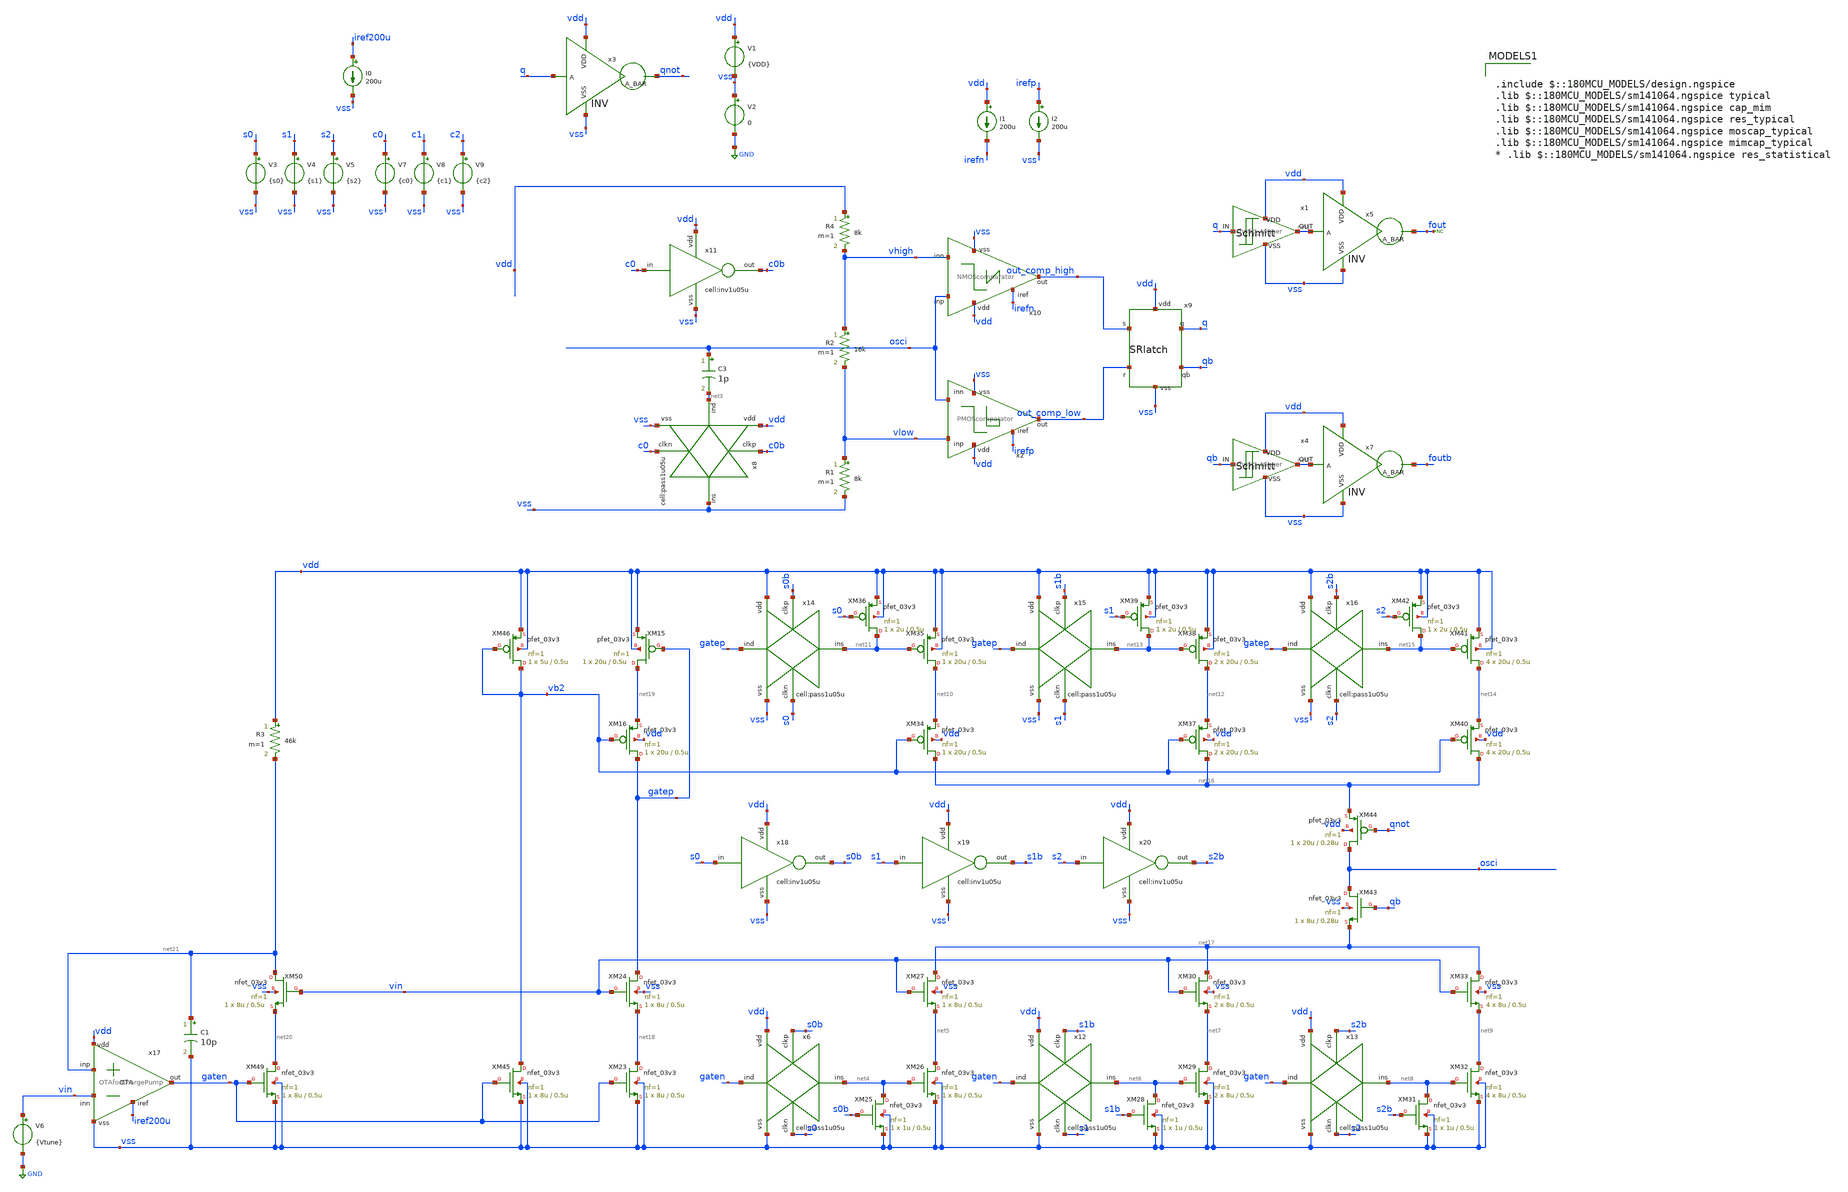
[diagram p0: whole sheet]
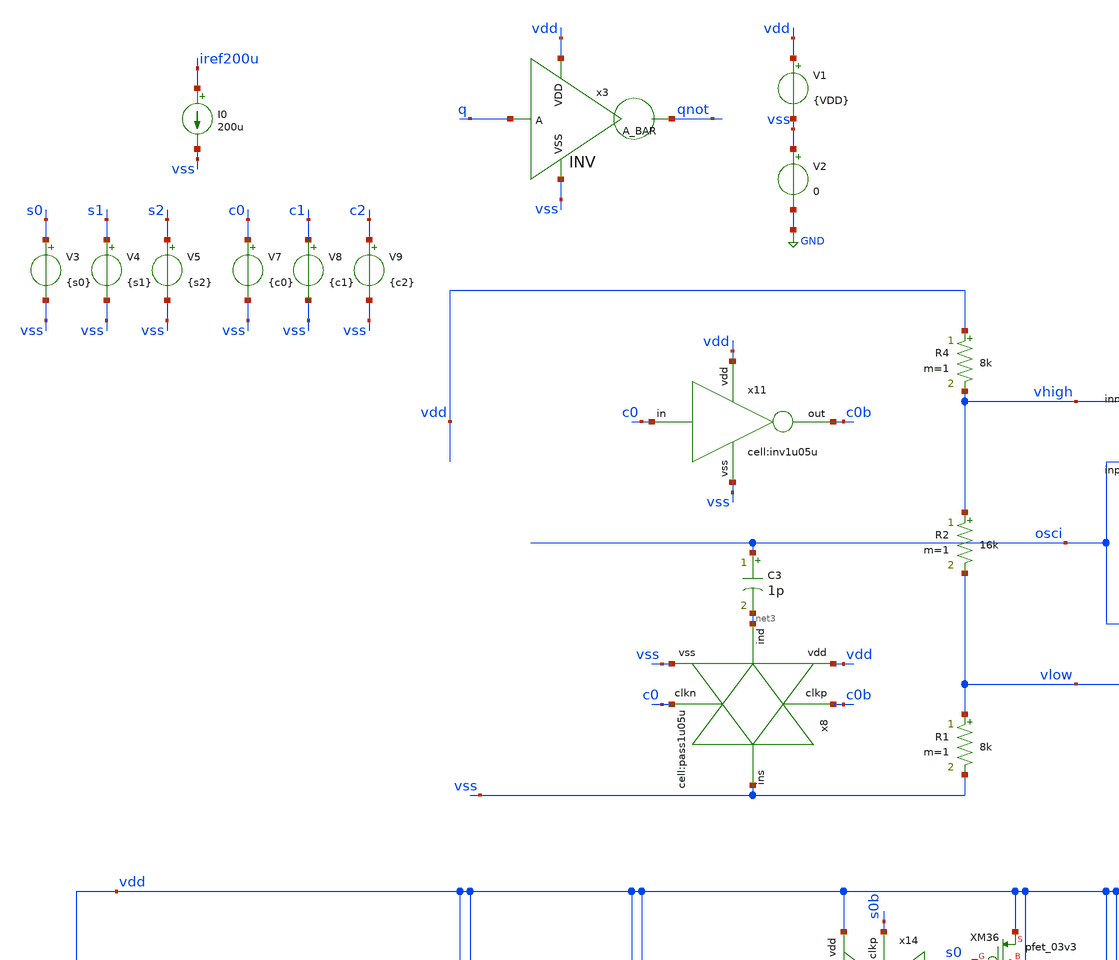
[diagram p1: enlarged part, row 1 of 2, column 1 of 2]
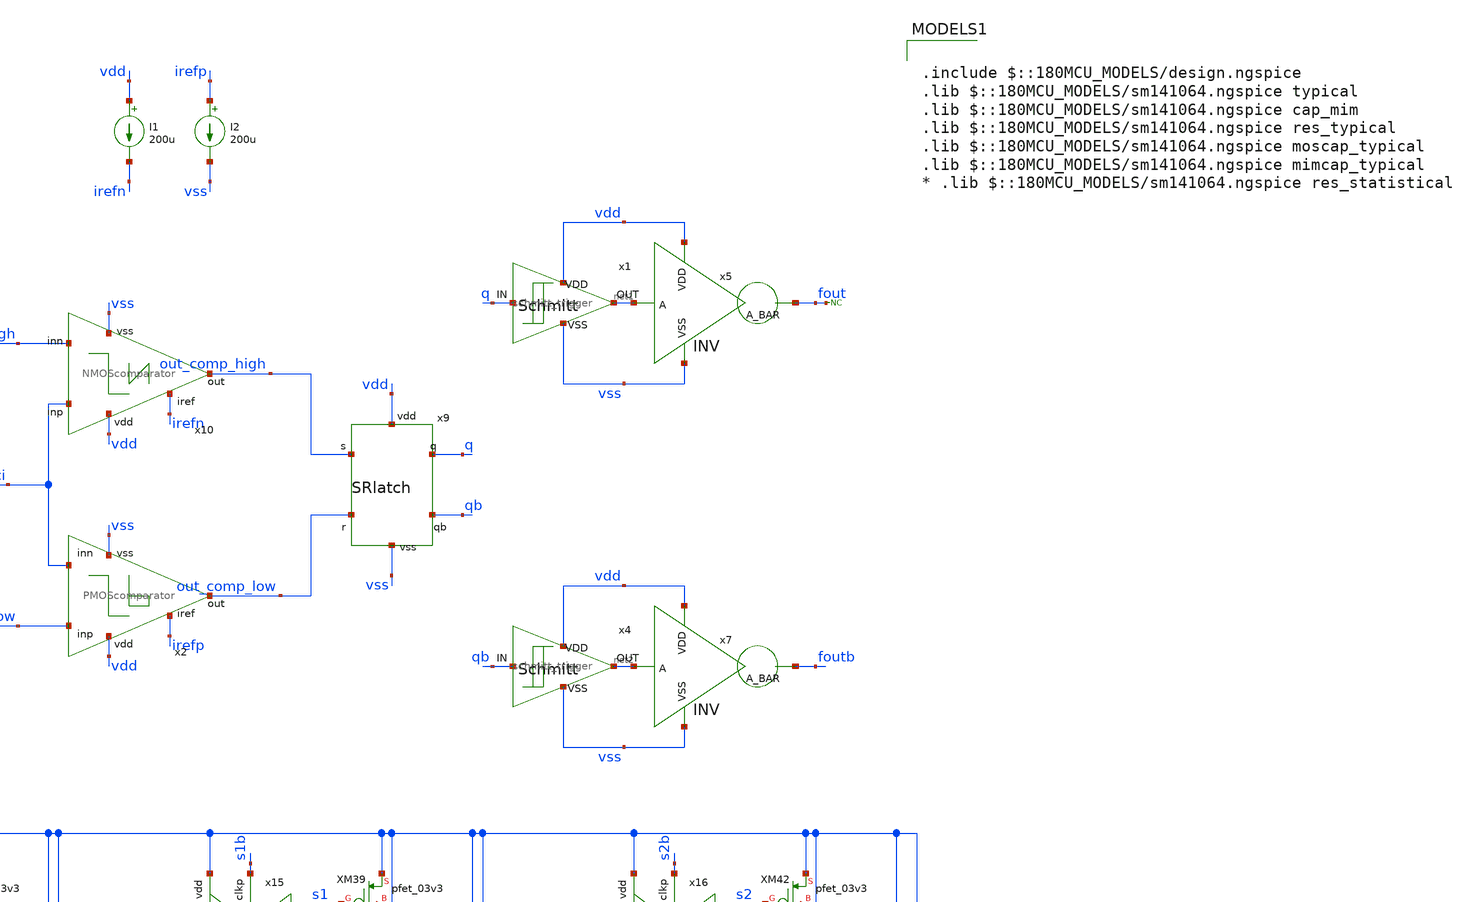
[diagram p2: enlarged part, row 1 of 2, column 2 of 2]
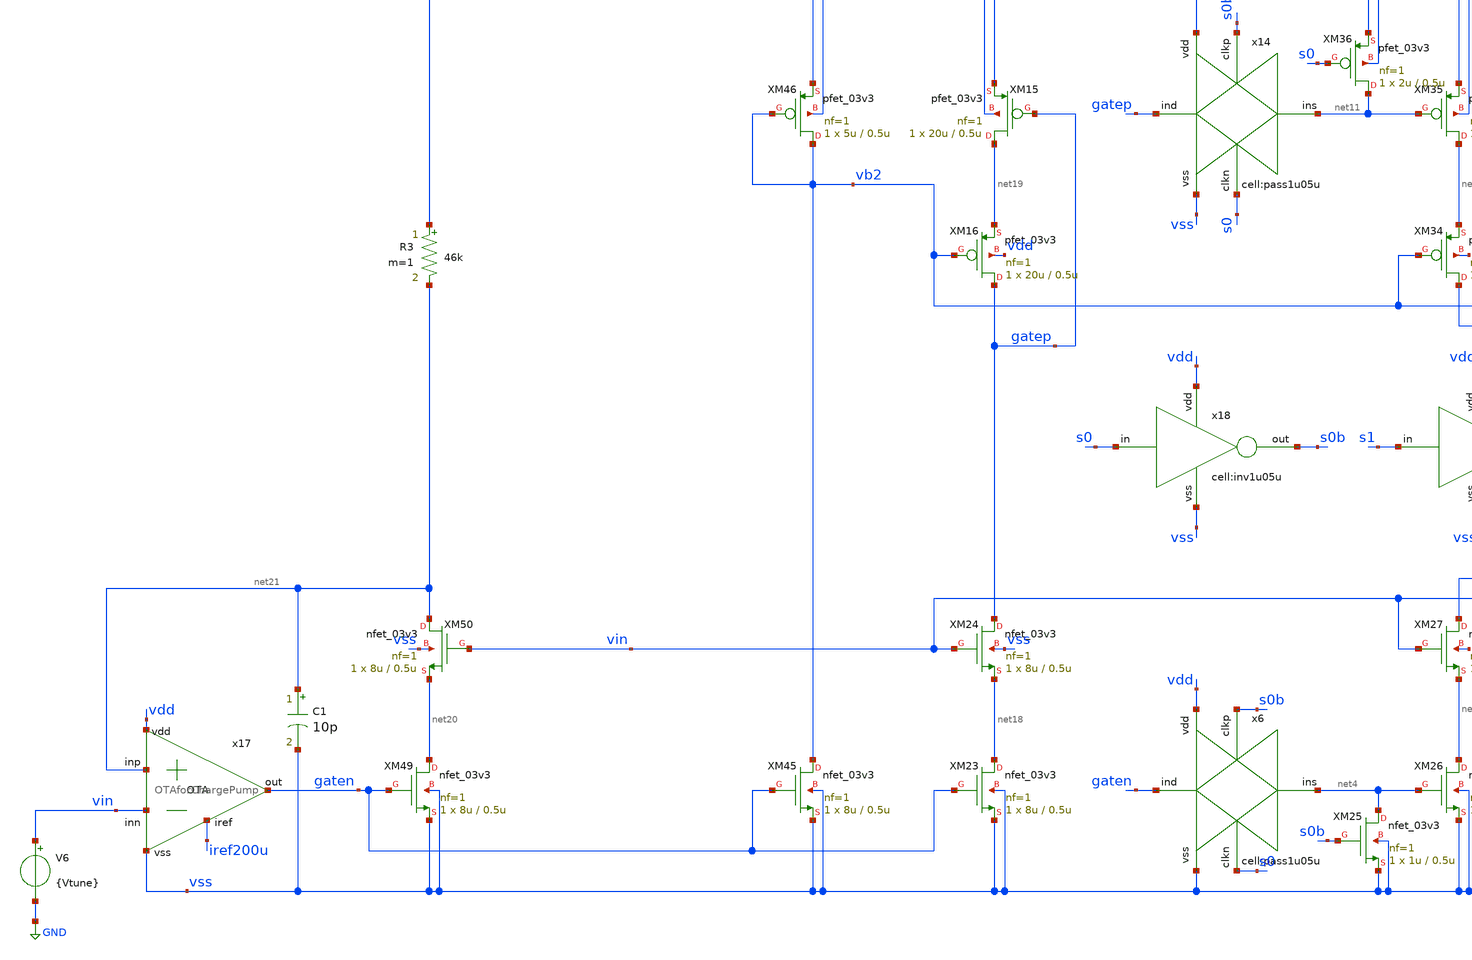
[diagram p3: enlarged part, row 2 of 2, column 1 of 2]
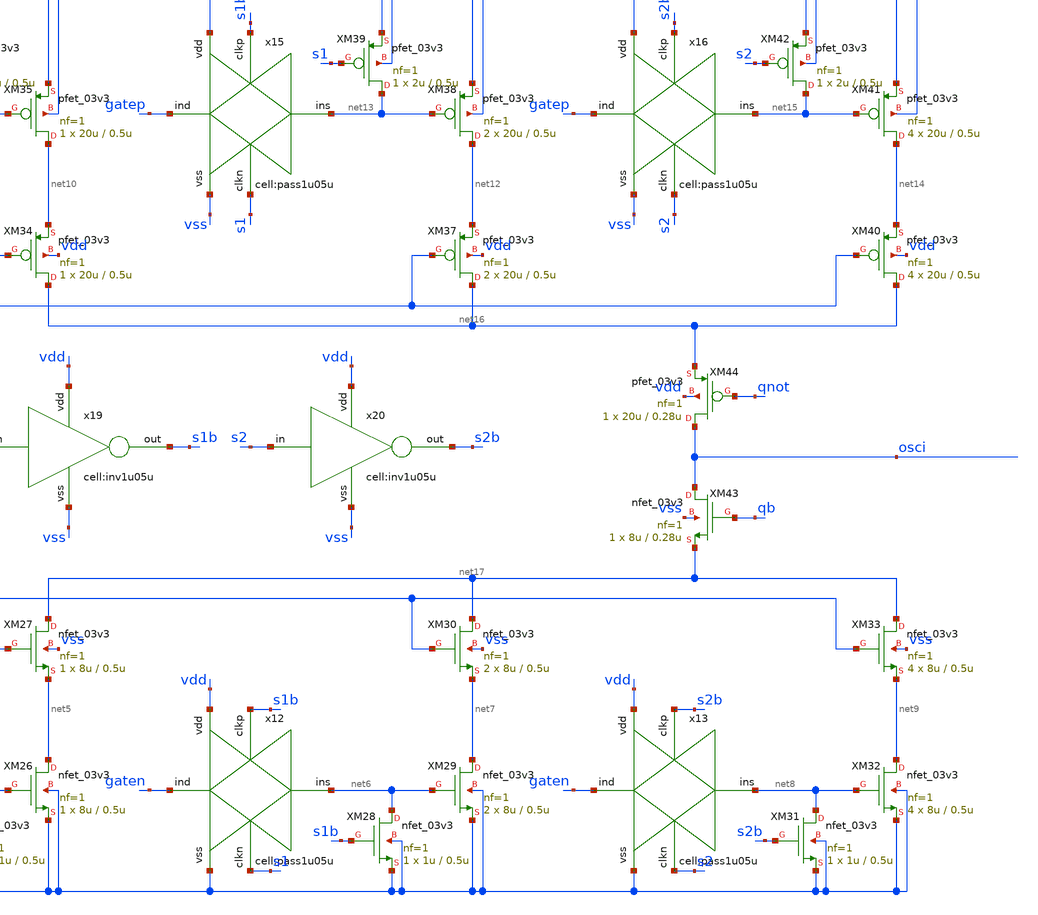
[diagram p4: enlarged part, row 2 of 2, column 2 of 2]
** sch_path: designs/libs/qw_core_analog/VCO0826/VCO0826.sch
**.subckt VCO0826
V1 vdd vss {VDD}
V2 vss GND 0
I1 vdd irefn 200u
I2 irefp vss 200u
R1 vlow vss 8k m=1
R2 vhigh vlow 16k m=1
R4 vdd vhigh 8k m=1
x9 vdd out_comp_high q qb out_comp_low vss SRlatch
x2 vdd irefp vlow out_comp_low osci vss PMOScomparator
x10 vdd osci out_comp_high vhigh irefn vss NMOScomparator
x3 vdd q qnot vss INV
x1 q net1 vdd vss schmitt_trigger
x4 qb net2 vdd vss schmitt_trigger
x5 vdd net1 fout vss INV
x7 vdd net2 foutb vss INV
V6 vin GND {Vtune}
I0 iref200u vss 200u
* noconn fout
V3 s0 vss {s0}
V4 s1 vss {s1}
V5 s2 vss {s2}
V7 c0 vss {c0}
V8 c1 vss {c1}
V9 c2 vss {c2}
C3 osci net3 1p m=1
x8 net3 vss c0 vss c0b vdd pass1u05u
x11 c0 vdd c0b vss inv1u05u
x6 gaten vss s0 net4 s0b vdd pass1u05u
XM25 net4 s0b vss vss nfet_03v3 L=0.5u W=1u nf=1 ad='int((nf+1)/2) * W/nf * 0.18u' as='int((nf+2)/2) * W/nf * 0.18u'
+ pd='2*int((nf+1)/2) * (W/nf + 0.18u)' ps='2*int((nf+2)/2) * (W/nf + 0.18u)' nrd='0.18u / W' nrs='0.18u / W'
+ sa=0 sb=0 sd=0 m=1
XM26 net5 net4 vss vss nfet_03v3 L=0.5u W=8u nf=1 ad='int((nf+1)/2) * W/nf * 0.18u' as='int((nf+2)/2) * W/nf * 0.18u'
+ pd='2*int((nf+1)/2) * (W/nf + 0.18u)' ps='2*int((nf+2)/2) * (W/nf + 0.18u)' nrd='0.18u / W' nrs='0.18u / W'
+ sa=0 sb=0 sd=0 m=1
XM27 net17 vin net5 vss nfet_03v3 L=0.5u W=8u nf=1 ad='int((nf+1)/2) * W/nf * 0.18u' as='int((nf+2)/2) * W/nf * 0.18u'
+ pd='2*int((nf+1)/2) * (W/nf + 0.18u)' ps='2*int((nf+2)/2) * (W/nf + 0.18u)' nrd='0.18u / W' nrs='0.18u / W'
+ sa=0 sb=0 sd=0 m=1
x12 gaten vss s1 net6 s1b vdd pass1u05u
XM28 net6 s1b vss vss nfet_03v3 L=0.5u W=1u nf=1 ad='int((nf+1)/2) * W/nf * 0.18u' as='int((nf+2)/2) * W/nf * 0.18u'
+ pd='2*int((nf+1)/2) * (W/nf + 0.18u)' ps='2*int((nf+2)/2) * (W/nf + 0.18u)' nrd='0.18u / W' nrs='0.18u / W'
+ sa=0 sb=0 sd=0 m=1
XM29 net7 net6 vss vss nfet_03v3 L=0.5u W=8u nf=1 ad='int((nf+1)/2) * W/nf * 0.18u' as='int((nf+2)/2) * W/nf * 0.18u'
+ pd='2*int((nf+1)/2) * (W/nf + 0.18u)' ps='2*int((nf+2)/2) * (W/nf + 0.18u)' nrd='0.18u / W' nrs='0.18u / W'
+ sa=0 sb=0 sd=0 m=2
XM30 net17 vin net7 vss nfet_03v3 L=0.5u W=8u nf=1 ad='int((nf+1)/2) * W/nf * 0.18u' as='int((nf+2)/2) * W/nf * 0.18u'
+ pd='2*int((nf+1)/2) * (W/nf + 0.18u)' ps='2*int((nf+2)/2) * (W/nf + 0.18u)' nrd='0.18u / W' nrs='0.18u / W'
+ sa=0 sb=0 sd=0 m=2
x13 gaten vss s2 net8 s2b vdd pass1u05u
XM31 net8 s2b vss vss nfet_03v3 L=0.5u W=1u nf=1 ad='int((nf+1)/2) * W/nf * 0.18u' as='int((nf+2)/2) * W/nf * 0.18u'
+ pd='2*int((nf+1)/2) * (W/nf + 0.18u)' ps='2*int((nf+2)/2) * (W/nf + 0.18u)' nrd='0.18u / W' nrs='0.18u / W'
+ sa=0 sb=0 sd=0 m=1
XM32 net9 net8 vss vss nfet_03v3 L=0.5u W=8u nf=1 ad='int((nf+1)/2) * W/nf * 0.18u' as='int((nf+2)/2) * W/nf * 0.18u'
+ pd='2*int((nf+1)/2) * (W/nf + 0.18u)' ps='2*int((nf+2)/2) * (W/nf + 0.18u)' nrd='0.18u / W' nrs='0.18u / W'
+ sa=0 sb=0 sd=0 m=4
XM33 net17 vin net9 vss nfet_03v3 L=0.5u W=8u nf=1 ad='int((nf+1)/2) * W/nf * 0.18u' as='int((nf+2)/2) * W/nf * 0.18u'
+ pd='2*int((nf+1)/2) * (W/nf + 0.18u)' ps='2*int((nf+2)/2) * (W/nf + 0.18u)' nrd='0.18u / W' nrs='0.18u / W'
+ sa=0 sb=0 sd=0 m=4
XM34 net16 vb2 net10 vdd pfet_03v3 L=0.5u W=20u nf=1 ad='int((nf+1)/2) * W/nf * 0.18u' as='int((nf+2)/2) * W/nf * 0.18u'
+ pd='2*int((nf+1)/2) * (W/nf + 0.18u)' ps='2*int((nf+2)/2) * (W/nf + 0.18u)' nrd='0.18u / W' nrs='0.18u / W'
+ sa=0 sb=0 sd=0 m=1
XM35 net10 net11 vdd vdd pfet_03v3 L=0.5u W=20u nf=1 ad='int((nf+1)/2) * W/nf * 0.18u' as='int((nf+2)/2) * W/nf * 0.18u'
+ pd='2*int((nf+1)/2) * (W/nf + 0.18u)' ps='2*int((nf+2)/2) * (W/nf + 0.18u)' nrd='0.18u / W' nrs='0.18u / W'
+ sa=0 sb=0 sd=0 m=1
x14 gatep vss s0 net11 s0b vdd pass1u05u
XM36 net11 s0 vdd vdd pfet_03v3 L=0.5u W=2u nf=1 ad='int((nf+1)/2) * W/nf * 0.18u' as='int((nf+2)/2) * W/nf * 0.18u'
+ pd='2*int((nf+1)/2) * (W/nf + 0.18u)' ps='2*int((nf+2)/2) * (W/nf + 0.18u)' nrd='0.18u / W' nrs='0.18u / W'
+ sa=0 sb=0 sd=0 m=1
XM37 net16 vb2 net12 vdd pfet_03v3 L=0.5u W=20u nf=1 ad='int((nf+1)/2) * W/nf * 0.18u' as='int((nf+2)/2) * W/nf * 0.18u'
+ pd='2*int((nf+1)/2) * (W/nf + 0.18u)' ps='2*int((nf+2)/2) * (W/nf + 0.18u)' nrd='0.18u / W' nrs='0.18u / W'
+ sa=0 sb=0 sd=0 m=2
XM38 net12 net13 vdd vdd pfet_03v3 L=0.5u W=20u nf=1 ad='int((nf+1)/2) * W/nf * 0.18u' as='int((nf+2)/2) * W/nf * 0.18u'
+ pd='2*int((nf+1)/2) * (W/nf + 0.18u)' ps='2*int((nf+2)/2) * (W/nf + 0.18u)' nrd='0.18u / W' nrs='0.18u / W'
+ sa=0 sb=0 sd=0 m=2
x15 gatep vss s1 net13 s1b vdd pass1u05u
XM39 net13 s1 vdd vdd pfet_03v3 L=0.5u W=2u nf=1 ad='int((nf+1)/2) * W/nf * 0.18u' as='int((nf+2)/2) * W/nf * 0.18u'
+ pd='2*int((nf+1)/2) * (W/nf + 0.18u)' ps='2*int((nf+2)/2) * (W/nf + 0.18u)' nrd='0.18u / W' nrs='0.18u / W'
+ sa=0 sb=0 sd=0 m=1
XM40 net16 vb2 net14 vdd pfet_03v3 L=0.5u W=20u nf=1 ad='int((nf+1)/2) * W/nf * 0.18u' as='int((nf+2)/2) * W/nf * 0.18u'
+ pd='2*int((nf+1)/2) * (W/nf + 0.18u)' ps='2*int((nf+2)/2) * (W/nf + 0.18u)' nrd='0.18u / W' nrs='0.18u / W'
+ sa=0 sb=0 sd=0 m=4
XM41 net14 net15 vdd vdd pfet_03v3 L=0.5u W=20u nf=1 ad='int((nf+1)/2) * W/nf * 0.18u' as='int((nf+2)/2) * W/nf * 0.18u'
+ pd='2*int((nf+1)/2) * (W/nf + 0.18u)' ps='2*int((nf+2)/2) * (W/nf + 0.18u)' nrd='0.18u / W' nrs='0.18u / W'
+ sa=0 sb=0 sd=0 m=4
x16 gatep vss s2 net15 s2b vdd pass1u05u
XM42 net15 s2 vdd vdd pfet_03v3 L=0.5u W=2u nf=1 ad='int((nf+1)/2) * W/nf * 0.18u' as='int((nf+2)/2) * W/nf * 0.18u'
+ pd='2*int((nf+1)/2) * (W/nf + 0.18u)' ps='2*int((nf+2)/2) * (W/nf + 0.18u)' nrd='0.18u / W' nrs='0.18u / W'
+ sa=0 sb=0 sd=0 m=1
XM43 osci qb net17 vss nfet_03v3 L=0.28u W=8u nf=1 ad='int((nf+1)/2) * W/nf * 0.18u' as='int((nf+2)/2) * W/nf * 0.18u'
+ pd='2*int((nf+1)/2) * (W/nf + 0.18u)' ps='2*int((nf+2)/2) * (W/nf + 0.18u)' nrd='0.18u / W' nrs='0.18u / W'
+ sa=0 sb=0 sd=0 m=1
XM44 osci qnot net16 vdd pfet_03v3 L=0.28u W=20u nf=1 ad='int((nf+1)/2) * W/nf * 0.18u' as='int((nf+2)/2) * W/nf * 0.18u'
+ pd='2*int((nf+1)/2) * (W/nf + 0.18u)' ps='2*int((nf+2)/2) * (W/nf + 0.18u)' nrd='0.18u / W' nrs='0.18u / W'
+ sa=0 sb=0 sd=0 m=1
XM15 net19 gatep vdd vdd pfet_03v3 L=0.5u W=20u nf=1 ad='int((nf+1)/2) * W/nf * 0.18u' as='int((nf+2)/2) * W/nf * 0.18u'
+ pd='2*int((nf+1)/2) * (W/nf + 0.18u)' ps='2*int((nf+2)/2) * (W/nf + 0.18u)' nrd='0.18u / W' nrs='0.18u / W'
+ sa=0 sb=0 sd=0 m=1
XM16 gatep vb2 net19 vdd pfet_03v3 L=0.5u W=20u nf=1 ad='int((nf+1)/2) * W/nf * 0.18u' as='int((nf+2)/2) * W/nf * 0.18u'
+ pd='2*int((nf+1)/2) * (W/nf + 0.18u)' ps='2*int((nf+2)/2) * (W/nf + 0.18u)' nrd='0.18u / W' nrs='0.18u / W'
+ sa=0 sb=0 sd=0 m=1
XM23 net18 gaten vss vss nfet_03v3 L=0.5u W=8u nf=1 ad='int((nf+1)/2) * W/nf * 0.18u' as='int((nf+2)/2) * W/nf * 0.18u'
+ pd='2*int((nf+1)/2) * (W/nf + 0.18u)' ps='2*int((nf+2)/2) * (W/nf + 0.18u)' nrd='0.18u / W' nrs='0.18u / W'
+ sa=0 sb=0 sd=0 m=1
XM24 gatep vin net18 vss nfet_03v3 L=0.5u W=8u nf=1 ad='int((nf+1)/2) * W/nf * 0.18u' as='int((nf+2)/2) * W/nf * 0.18u'
+ pd='2*int((nf+1)/2) * (W/nf + 0.18u)' ps='2*int((nf+2)/2) * (W/nf + 0.18u)' nrd='0.18u / W' nrs='0.18u / W'
+ sa=0 sb=0 sd=0 m=1
XM45 vb2 gaten vss vss nfet_03v3 L=0.5u W=8u nf=1 ad='int((nf+1)/2) * W/nf * 0.18u' as='int((nf+2)/2) * W/nf * 0.18u'
+ pd='2*int((nf+1)/2) * (W/nf + 0.18u)' ps='2*int((nf+2)/2) * (W/nf + 0.18u)' nrd='0.18u / W' nrs='0.18u / W'
+ sa=0 sb=0 sd=0 m=1
XM46 vb2 vb2 vdd vdd pfet_03v3 L=0.5u W=5u nf=1 ad='int((nf+1)/2) * W/nf * 0.18u' as='int((nf+2)/2) * W/nf * 0.18u'
+ pd='2*int((nf+1)/2) * (W/nf + 0.18u)' ps='2*int((nf+2)/2) * (W/nf + 0.18u)' nrd='0.18u / W' nrs='0.18u / W'
+ sa=0 sb=0 sd=0 m=1
XM49 net20 gaten vss vss nfet_03v3 L=0.5u W=8u nf=1 ad='int((nf+1)/2) * W/nf * 0.18u' as='int((nf+2)/2) * W/nf * 0.18u'
+ pd='2*int((nf+1)/2) * (W/nf + 0.18u)' ps='2*int((nf+2)/2) * (W/nf + 0.18u)' nrd='0.18u / W' nrs='0.18u / W'
+ sa=0 sb=0 sd=0 m=1
XM50 net21 vin net20 vss nfet_03v3 L=0.5u W=8u nf=1 ad='int((nf+1)/2) * W/nf * 0.18u' as='int((nf+2)/2) * W/nf * 0.18u'
+ pd='2*int((nf+1)/2) * (W/nf + 0.18u)' ps='2*int((nf+2)/2) * (W/nf + 0.18u)' nrd='0.18u / W' nrs='0.18u / W'
+ sa=0 sb=0 sd=0 m=1
x17 vdd iref200u net21 vin gaten vss OTAforChargePump
R3 vdd net21 46k m=1
x18 s0 vdd s0b vss inv1u05u
x19 s1 vdd s1b vss inv1u05u
x20 s2 vdd s2b vss inv1u05u
C1 net21 vss 10p m=1
**** begin user architecture code



.param VDD = 3.3
.param Vtune = 2.7
.param s0 = 3.3 s1 = 3.3 s2 = 3.3 c0 = 0 c1 = 0 c2 = 3.3
.param VIN=1
*V6 net3 0 {Vtune}
.meas tran period1 TRIG v(fout) VAL=1.65 RISE=15 TARG v(fout) VAL=1.65 RISE=16
.meas tran freq param='1/period1'

.control
save all

let vstart = 0.0
let vstop = 3.3
let vstep = 0.1

foreach VINVAL 2.1 2.2
    alterparam Vtune = $VINVAL
    reset
    tran 10p 100n
end

write VCO0818.raw
.endc



.include $::180MCU_MODELS/design.ngspice
.lib $::180MCU_MODELS/sm141064.ngspice typical
.lib $::180MCU_MODELS/sm141064.ngspice cap_mim
.lib $::180MCU_MODELS/sm141064.ngspice res_typical
.lib $::180MCU_MODELS/sm141064.ngspice moscap_typical
.lib $::180MCU_MODELS/sm141064.ngspice mimcap_typical
* .lib $::180MCU_MODELS/sm141064.ngspice res_statistical

**** end user architecture code
**.ends
.GLOBAL GND
.end
